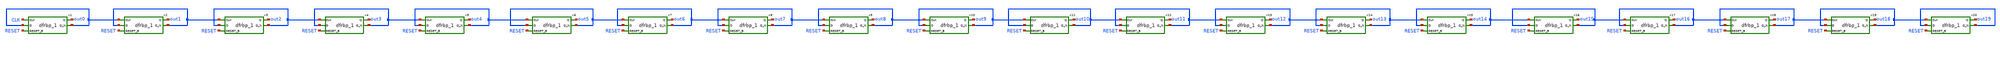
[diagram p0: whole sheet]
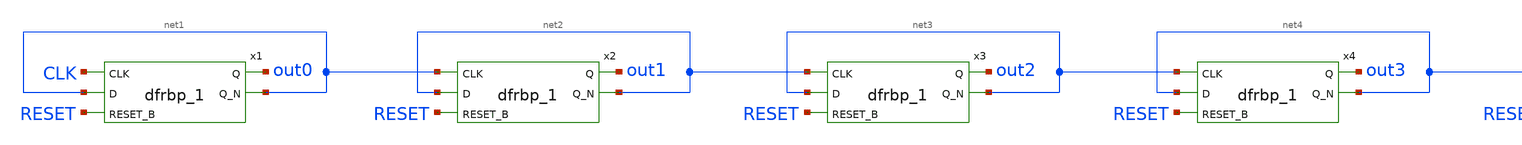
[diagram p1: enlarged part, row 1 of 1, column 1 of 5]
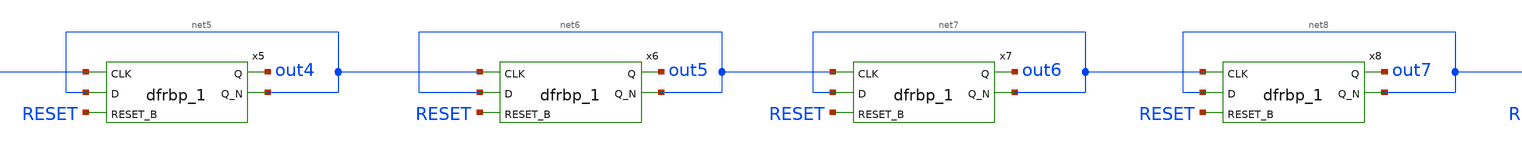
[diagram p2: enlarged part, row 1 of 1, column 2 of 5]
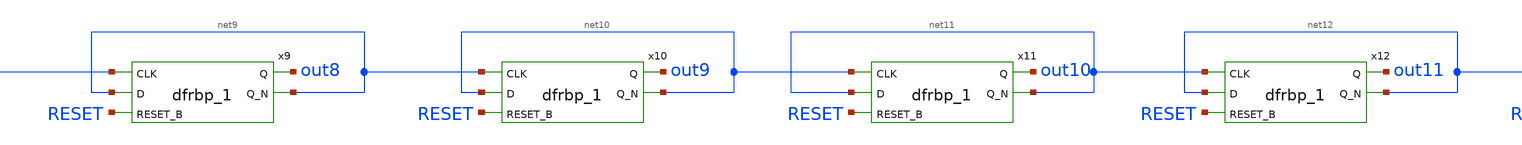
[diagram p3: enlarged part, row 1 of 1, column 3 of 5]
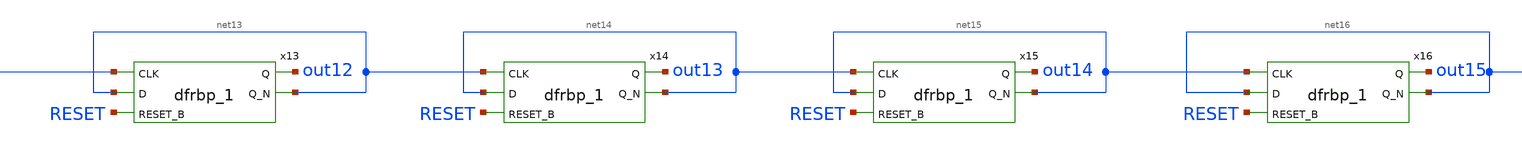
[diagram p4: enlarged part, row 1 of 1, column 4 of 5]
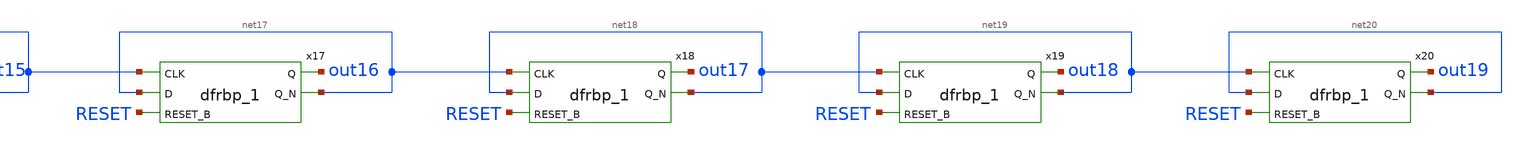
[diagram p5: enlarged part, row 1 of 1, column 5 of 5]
** sch_path: Schematics/Counter/20bitCounter.sch
**.subckt 20bitCounter
x1 CLK net1 RESET GND VDD out0 net1 sky130_fd_sc_hd__dfrbp_1
x2 net1 net2 RESET GND VDD out1 net2 sky130_fd_sc_hd__dfrbp_1
x3 net2 net3 RESET GND VDD out2 net3 sky130_fd_sc_hd__dfrbp_1
x4 net3 net4 RESET GND VDD out3 net4 sky130_fd_sc_hd__dfrbp_1
x5 net4 net5 RESET GND VDD out4 net5 sky130_fd_sc_hd__dfrbp_1
x6 net5 net6 RESET GND VDD out5 net6 sky130_fd_sc_hd__dfrbp_1
x7 net6 net7 RESET GND VDD out6 net7 sky130_fd_sc_hd__dfrbp_1
x8 net7 net8 RESET GND VDD out7 net8 sky130_fd_sc_hd__dfrbp_1
x9 net8 net9 RESET GND VDD out8 net9 sky130_fd_sc_hd__dfrbp_1
x10 net9 net10 RESET GND VDD out9 net10 sky130_fd_sc_hd__dfrbp_1
x11 net10 net11 RESET GND VDD out10 net11 sky130_fd_sc_hd__dfrbp_1
x12 net11 net12 RESET GND VDD out11 net12 sky130_fd_sc_hd__dfrbp_1
x13 net12 net13 RESET GND VDD out12 net13 sky130_fd_sc_hd__dfrbp_1
x14 net13 net14 RESET GND VDD out13 net14 sky130_fd_sc_hd__dfrbp_1
x15 net14 net15 RESET GND VDD out14 net15 sky130_fd_sc_hd__dfrbp_1
x16 net15 net16 RESET GND VDD out15 net16 sky130_fd_sc_hd__dfrbp_1
x17 net16 net17 RESET GND VDD out16 net17 sky130_fd_sc_hd__dfrbp_1
x18 net17 net18 RESET GND VDD out17 net18 sky130_fd_sc_hd__dfrbp_1
x19 net18 net19 RESET GND VDD out18 net19 sky130_fd_sc_hd__dfrbp_1
x20 net19 net20 RESET GND VDD out19 net20 sky130_fd_sc_hd__dfrbp_1
**** begin user architecture code
.lib ~/open_pdks/sky130/sky130A/libs.tech/ngspice/sky130.lib.spice tt
.include ~/Documents/counter/layout/lvs_check/tempFix/poseEdge_Dff.spice
**** end user architecture code
**.ends
.end
